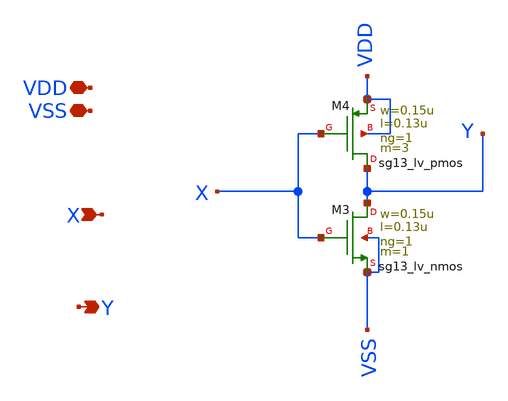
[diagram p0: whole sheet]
** sch_path: xschem/DigitalGates/INV.sch
**.subckt INV VDD X Y VSS
*.iopin VDD
*.ipin X
*.opin Y
*.iopin VSS
XM3 Y X VSS VSS sg13_lv_nmos w=0.15u l=0.13u ng=1 m=1 mm_ok=1
XM4 Y X VDD VDD sg13_lv_pmos w=0.15u l=0.13u ng=1 m=3 mm_ok=1
**** begin user architecture code



**** end user architecture code
**.ends
.end
